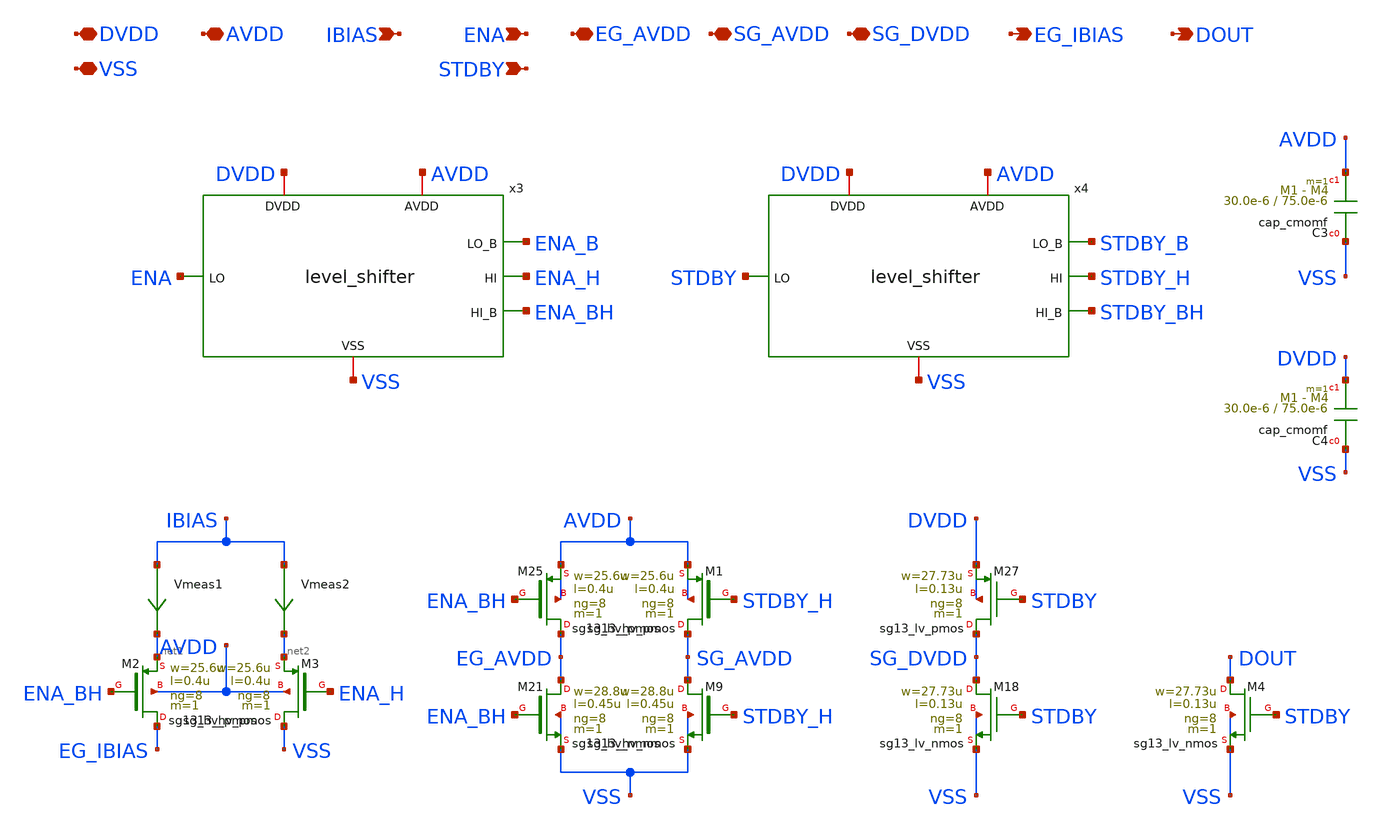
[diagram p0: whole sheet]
** sch_path: xschem/power_gating.sch
**.subckt power_gating DVDD VSS AVDD ENA STDBY DOUT IBIAS EG_AVDD SG_AVDD SG_DVDD EG_IBIAS
*.iopin DVDD
*.iopin VSS
*.iopin AVDD
*.ipin ENA
*.ipin STDBY
*.opin DOUT
*.ipin IBIAS
*.iopin EG_AVDD
*.iopin SG_AVDD
*.iopin SG_DVDD
*.opin EG_IBIAS
x3 AVDD ENA_B DVDD ENA ENA_H VSS ENA_BH level_shifter
x4 AVDD STDBY_B DVDD STDBY STDBY_H VSS STDBY_BH level_shifter
XC3 VSS AVDD cap_cmomf w=30.0e-6 l=75.0e-6 mmin=1 mmax=4 subblock=0 rfmodel=0 subscale=1 m=1 mm_ok=1
XC4 VSS DVDD cap_cmomf w=30.0e-6 l=75.0e-6 mmin=1 mmax=4 subblock=0 rfmodel=0 subscale=1 m=1 mm_ok=1
XM2 EG_IBIAS ENA_BH net1 AVDD sg13_hv_pmos w=25.6u l=0.4u ng=8 m=1 mm_ok=1
XM1 SG_AVDD STDBY_H AVDD AVDD sg13_hv_pmos w=25.6u l=0.4u ng=8 m=1 mm_ok=1
XM25 EG_AVDD ENA_BH AVDD AVDD sg13_hv_pmos w=25.6u l=0.4u ng=8 m=1 mm_ok=1
XM9 SG_AVDD STDBY_H VSS VSS sg13_hv_nmos w=28.8u l=0.45u ng=8 m=1 mm_ok=1
XM21 EG_AVDD ENA_BH VSS VSS sg13_hv_nmos w=28.8u l=0.45u ng=8 m=1 mm_ok=1
XM27 SG_DVDD STDBY DVDD DVDD sg13_lv_pmos w=27.73u l=0.13u ng=8 m=1 mm_ok=1
XM18 SG_DVDD STDBY VSS VSS sg13_lv_nmos w=27.73u l=0.13u ng=8 m=1 mm_ok=1
XM4 DOUT STDBY VSS VSS sg13_lv_nmos w=27.73u l=0.13u ng=8 m=1 mm_ok=1
Vmeas1 IBIAS net1 0
.save i(vmeas1)
Vmeas2 IBIAS net2 0
.save i(vmeas2)
XM3 VSS ENA_H net2 AVDD sg13_hv_pmos w=25.6u l=0.4u ng=8 m=1 mm_ok=1
**.ends

* expanding   symbol:  level_shifter.sym # of pins=7
** sym_path: xschem/level_shifter.sym
** sch_path: xschem/level_shifter.sch
.subckt level_shifter AVDD LO_B DVDD LO HI VSS HI_B
*.iopin DVDD
*.iopin VSS
*.iopin AVDD
*.ipin LO
*.opin LO_B
*.opin HI
*.opin HI_B
XM1 IM_B IM AVDD AVDD sg13_hv_pmos w=0.8u l=0.4u ng=1 m=1 mm_ok=1
XM2 IM_B LO_BB VSS VSS sg13_hv_nmos w=0.9u l=0.45u ng=1 m=1 mm_ok=1
XM3 IM IM_B AVDD AVDD sg13_hv_pmos w=0.8u l=0.4u ng=1 m=1 mm_ok=1
XM4 IM LO_B VSS VSS sg13_hv_nmos w=0.9u l=0.45u ng=1 m=1 mm_ok=1
XM5 LO_B LO DVDD DVDD sg13_lv_pmos w=0.87u l=0.13u ng=1 m=1 mm_ok=1
XM6 LO_B LO VSS VSS sg13_lv_nmos w=0.87u l=0.13u ng=1 m=1 mm_ok=1
XM7 LO_BB LO_B DVDD DVDD sg13_lv_pmos w=0.87u l=0.13u ng=1 m=1 mm_ok=1
XM8 LO_BB LO_B VSS VSS sg13_lv_nmos w=0.87u l=0.13u ng=1 m=1 mm_ok=1
XM9 HI IM_B AVDD AVDD sg13_hv_pmos w=0.8u l=0.4u ng=1 m=1 mm_ok=1
XM10 HI IM_B VSS VSS sg13_hv_nmos w=0.9u l=0.45u ng=1 m=1 mm_ok=1
XM11 HI_B HI AVDD AVDD sg13_hv_pmos w=0.8u l=0.4u ng=1 m=1 mm_ok=1
XM12 HI_B HI VSS VSS sg13_hv_nmos w=0.9u l=0.45u ng=1 m=1 mm_ok=1
.ends

.end
